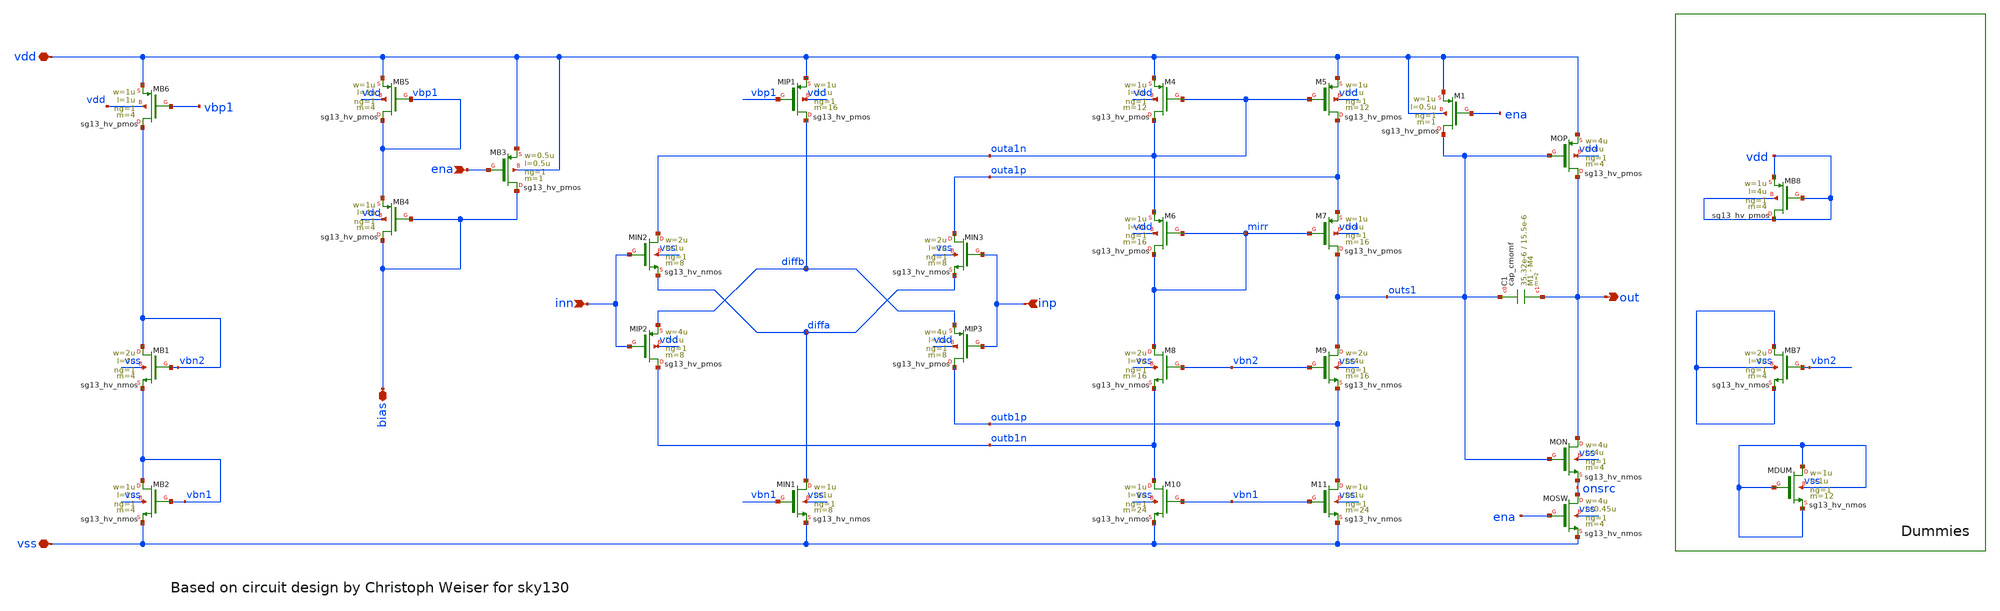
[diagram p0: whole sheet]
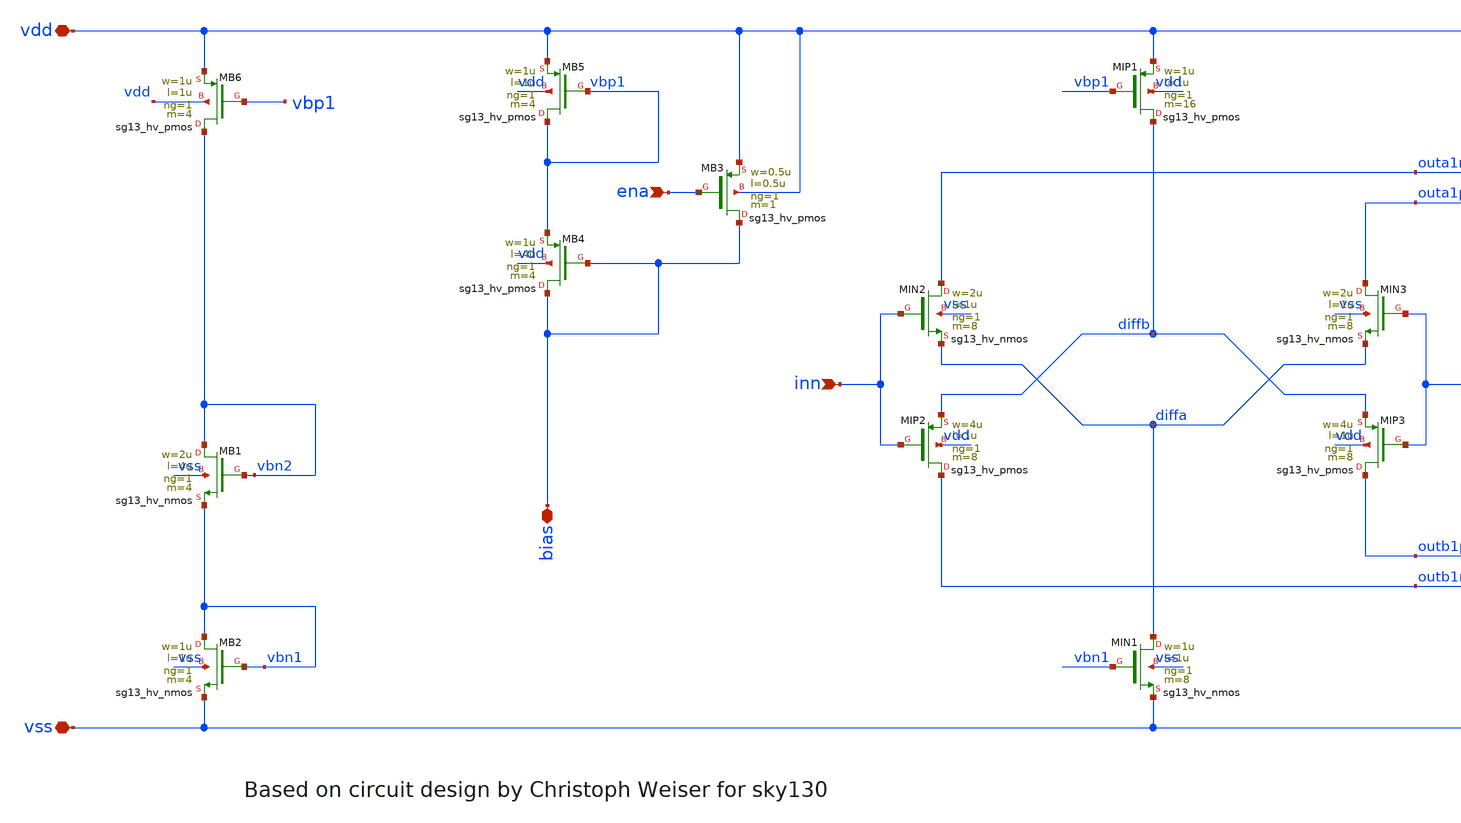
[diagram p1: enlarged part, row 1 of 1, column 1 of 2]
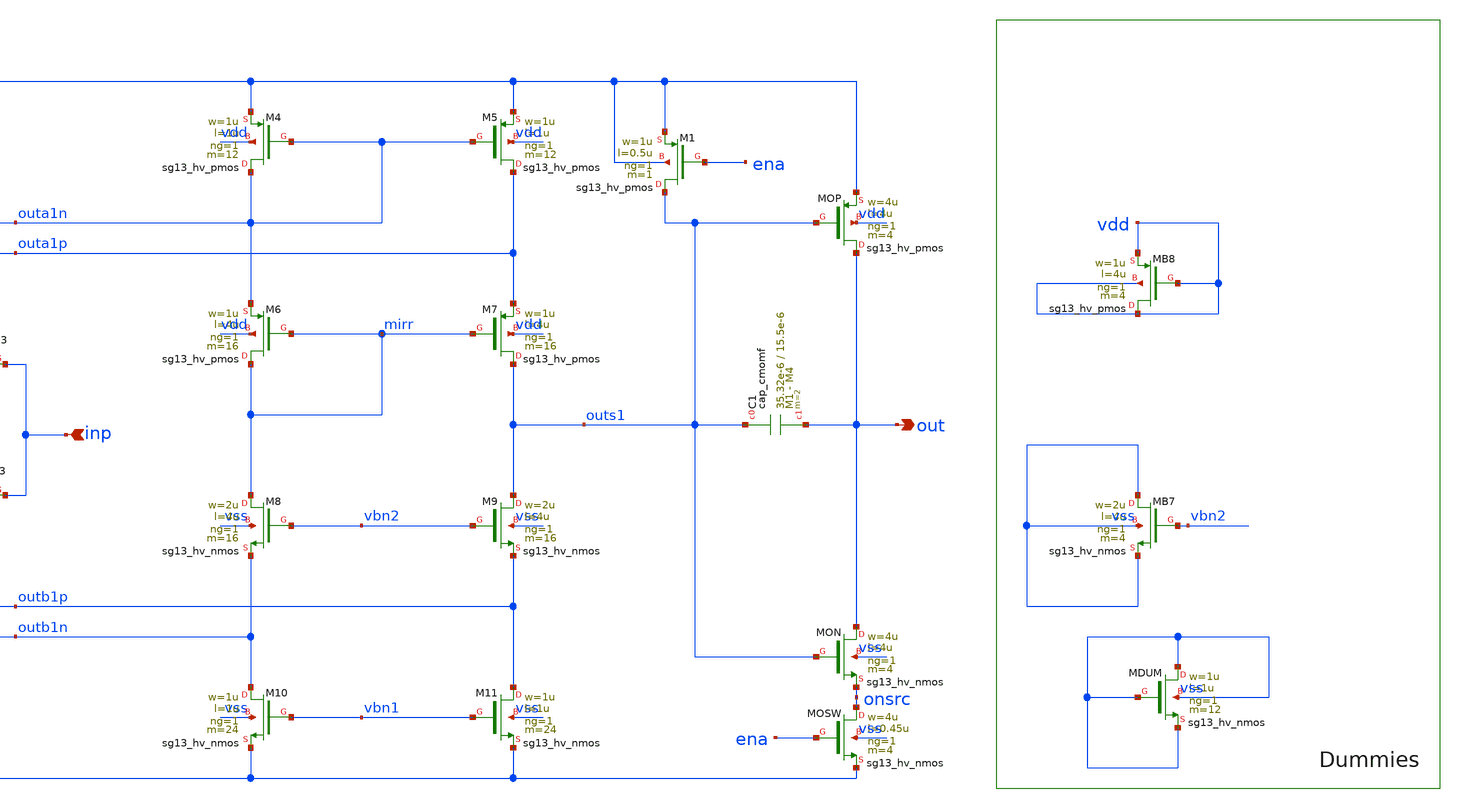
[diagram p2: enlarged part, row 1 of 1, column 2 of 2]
** sch_path: xschem/se_folded_cascode_np_ab.sch
**.subckt se_folded_cascode_np_ab vdd bias inp inn vss out ena
*.iopin vdd
*.iopin bias
*.ipin inp
*.ipin inn
*.iopin vss
*.opin out
*.ipin ena
XM4 outa1n outa1n vdd vdd sg13_hv_pmos w=1u l=1u ng=1 m=12 mm_ok=1
XM5 outa1p outa1n vdd vdd sg13_hv_pmos w=1u l=1u ng=1 m=12 mm_ok=1
XMIN1 diffa vbn1 vss vss sg13_hv_nmos w=1u l=1u ng=1 m=8 mm_ok=1
XMB2 vbn1 vbn1 vss vss sg13_hv_nmos w=1u l=1u ng=1 m=4 mm_ok=1
XMB1 vbn2 vbn2 vbn1 vss sg13_hv_nmos w=2u l=4u ng=1 m=4 mm_ok=1
XMIN2 outa1n inn diffa vss sg13_hv_nmos w=2u l=1u ng=1 m=8 mm_ok=1
XMIN3 outa1p inp diffa vss sg13_hv_nmos w=2u l=1u ng=1 m=8 mm_ok=1
XMB5 vbp1 vbp1 vdd vdd sg13_hv_pmos w=1u l=1u ng=1 m=4 mm_ok=1
XM7 outs1 mirr outa1p vdd sg13_hv_pmos w=1u l=4u ng=1 m=16 mm_ok=1
XM6 mirr mirr outa1n vdd sg13_hv_pmos w=1u l=4u ng=1 m=16 mm_ok=1
XM8 mirr vbn2 outb1n vss sg13_hv_nmos w=2u l=4u ng=1 m=16 mm_ok=1
XM9 outs1 vbn2 outb1p vss sg13_hv_nmos w=2u l=4u ng=1 m=16 mm_ok=1
XM10 outb1n vbn1 vss vss sg13_hv_nmos w=1u l=1u ng=1 m=24 mm_ok=1
XM11 outb1p vbn1 vss vss sg13_hv_nmos w=1u l=1u ng=1 m=24 mm_ok=1
XMB4 bias bias vbp1 vdd sg13_hv_pmos w=1u l=4u ng=1 m=4 mm_ok=1
XMIP2 outb1n inn diffb vdd sg13_hv_pmos w=4u l=1u ng=1 m=8 mm_ok=1
XMIP3 outb1p inp diffb vdd sg13_hv_pmos w=4u l=1u ng=1 m=8 mm_ok=1
XMIP1 diffb vbp1 vdd vdd sg13_hv_pmos w=1u l=1u ng=1 m=16 mm_ok=1
XMON out outs1 onsrc vss sg13_hv_nmos w=4u l=4u ng=1 m=4 mm_ok=1
XMOP out outs1 vdd vdd sg13_hv_pmos w=4u l=4u ng=1 m=4 mm_ok=1
XMB6 vbn2 vbp1 vdd vdd sg13_hv_pmos w=1u l=1u ng=1 m=4 mm_ok=1
XMDUM vss vss vss vss sg13_hv_nmos w=1u l=1u ng=1 m=12 mm_ok=1
XMB7 vss vbn2 vss vss sg13_hv_nmos w=2u l=4u ng=1 m=4 mm_ok=1
XC1 outs1 out cap_cmomf w=35.32e-6 l=15.5e-6 mmin=1 mmax=4 subblock=1 rfmodel=0 subscale=1 m=2
+ mm_ok=1
XMB3 bias ena vdd vdd sg13_hv_pmos w=0.5u l=0.5u ng=1 m=1 mm_ok=1
XMB8 vdd vdd vdd vdd sg13_hv_pmos w=1u l=4u ng=1 m=4 mm_ok=1
XMOSW onsrc ena vss vss sg13_hv_nmos w=4u l=0.45u ng=1 m=4 mm_ok=1
XM1 outs1 ena vdd vdd sg13_hv_pmos w=1u l=0.5u ng=1 m=1 mm_ok=1
**.ends
.end
